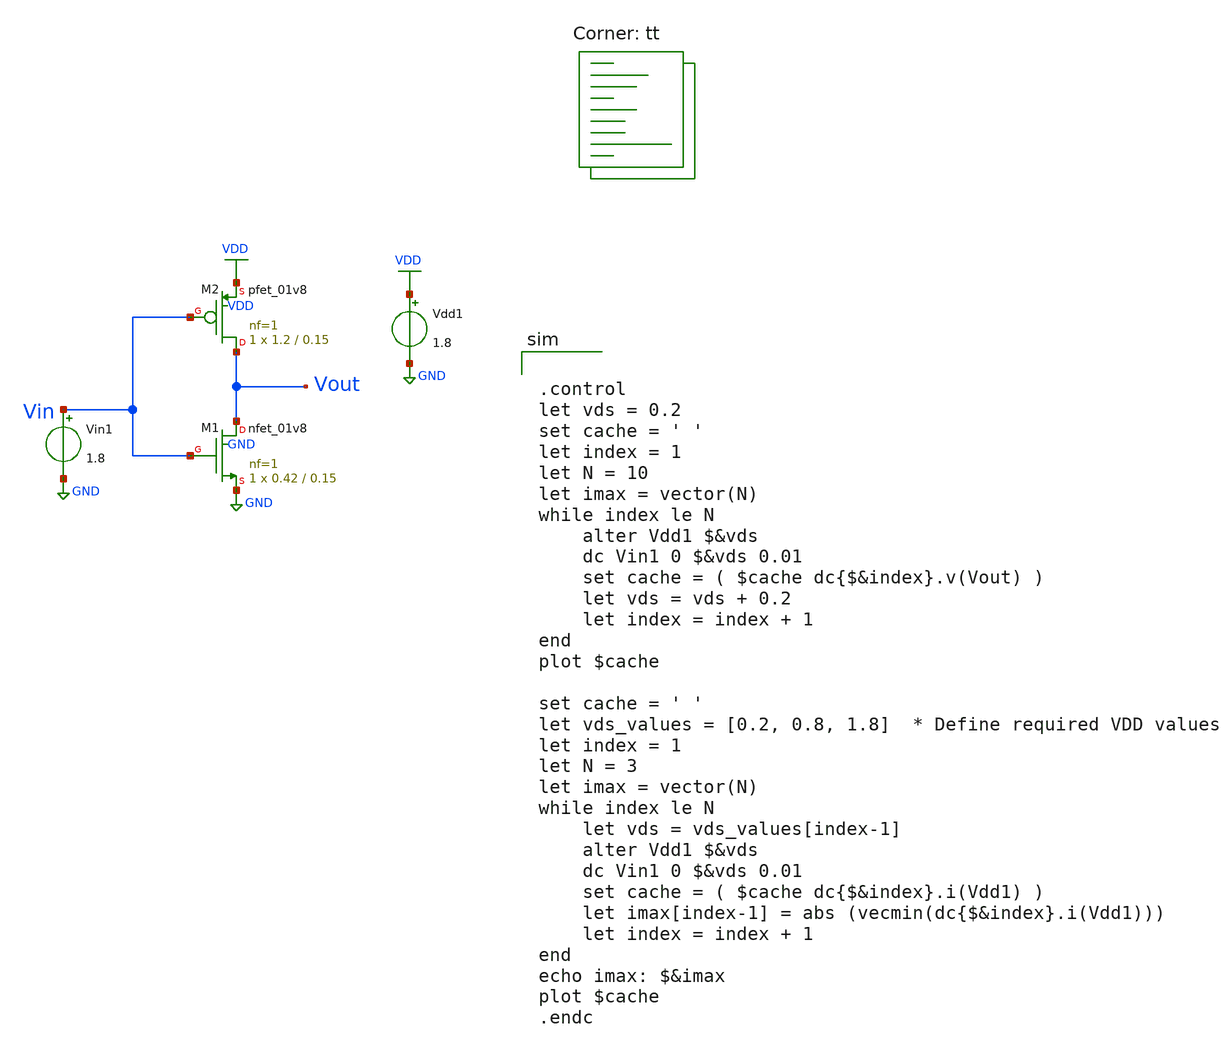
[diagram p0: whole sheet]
** sch_path: Tutorial_2/VTC_vs_VDD.sch
**.subckt VTC_vs_VDD
XM1 Vout Vin GND GND sky130_fd_pr__nfet_01v8 L=0.15 W=0.42 nf=1 ad='int((nf+1)/2) * W/nf * 0.29' as='int((nf+2)/2) * W/nf * 0.29'
+ pd='2*int((nf+1)/2) * (W/nf + 0.29)' ps='2*int((nf+2)/2) * (W/nf + 0.29)' nrd='0.29 / W' nrs='0.29 / W'
+ sa=0 sb=0 sd=0 mult=1 m=1
XM2 Vout Vin VDD VDD sky130_fd_pr__pfet_01v8 L=0.15 W=1.2 nf=1 ad='int((nf+1)/2) * W/nf * 0.29' as='int((nf+2)/2) * W/nf * 0.29'
+ pd='2*int((nf+1)/2) * (W/nf + 0.29)' ps='2*int((nf+2)/2) * (W/nf + 0.29)' nrd='0.29 / W' nrs='0.29 / W'
+ sa=0 sb=0 sd=0 mult=1 m=1
Vdd1 VDD GND 1.8
Vin1 Vin GND 1.8
**** begin user architecture code


.control
let vds = 0.2
set cache = ' '
let index = 1
let N = 10
let imax = vector(N)
while index le N
	alter Vdd1 $&vds
	dc Vin1 0 $&vds 0.01
	set cache = ( $cache dc{$&index}.v(Vout) )
	let vds = vds + 0.2
	let index = index + 1
end
plot $cache

set cache = ' '
let vds_values = [0.2, 0.8, 1.8]  * Define required VDD values
let index = 1
let N = 3
let imax = vector(N)
while index le N
	let vds = vds_values[index-1]
	alter Vdd1 $&vds
	dc Vin1 0 $&vds 0.01
	set cache = ( $cache dc{$&index}.i(Vdd1) )
	let imax[index-1] = abs (vecmin(dc{$&index}.i(Vdd1)))
	let index = index + 1
end
echo imax: $&imax
plot $cache
.endc


.lib $::SKYWATER_MODELS/sky130.lib.spice tt
**** end user architecture code
**.ends
.GLOBAL GND
.GLOBAL VDD
.end
